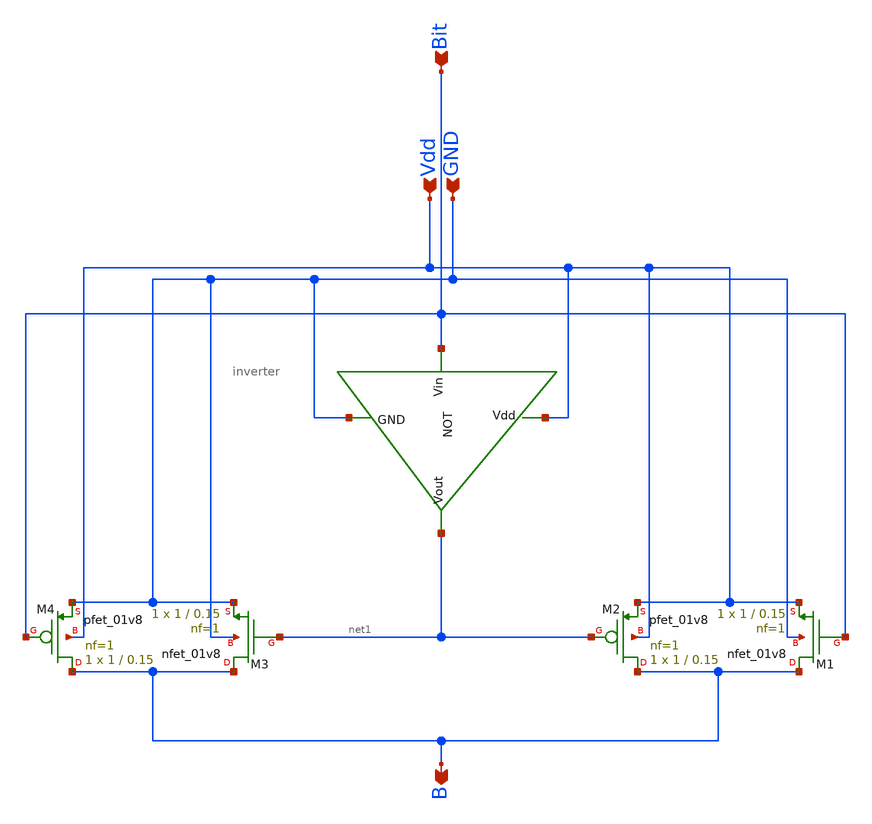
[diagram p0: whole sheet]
** sch_path: MUX_2to1.sch
**.subckt MUX_2to1 Bit Vdd GND B
*.ipin Bit
*.ipin Vdd
*.ipin GND
*.opin B
XM1 B Bit Vdd GND sky130_fd_pr__nfet_01v8 L=0.15 W=1 nf=1 ad='int((1 + 1)/2) * 1 / 1 * 0.29' as='int((1 + 2)/2) * 1 / 1 * 0.29'
+ pd='2*int((1 + 1)/2) * (1 / 1 + 0.29)' ps='2*int((1 + 2)/2) * (1 / 1 + 0.29)' nrd='0.29 / 1 ' nrs='0.29 / 1 '
+ sa=0 sb=0 sd=0 mult=1 m=1
XM2 B net1 Vdd Vdd sky130_fd_pr__pfet_01v8 L=0.15 W=1 nf=1 ad='int((1 + 1)/2) * 1 / 1 * 0.29' as='int((1 + 2)/2) * 1 / 1 * 0.29'
+ pd='2*int((1 + 1)/2) * (1 / 1 + 0.29)' ps='2*int((1 + 2)/2) * (1 / 1 + 0.29)' nrd='0.29 / 1 ' nrs='0.29 / 1 '
+ sa=0 sb=0 sd=0 mult=1 m=1
x1 Vdd Bit net1 GND inverter
XM3 B net1 GND GND sky130_fd_pr__nfet_01v8 L=0.15 W=1 nf=1 ad='int((1 + 1)/2) * 1 / 1 * 0.29' as='int((1 + 2)/2) * 1 / 1 * 0.29'
+ pd='2*int((1 + 1)/2) * (1 / 1 + 0.29)' ps='2*int((1 + 2)/2) * (1 / 1 + 0.29)' nrd='0.29 / 1 ' nrs='0.29 / 1 '
+ sa=0 sb=0 sd=0 mult=1 m=1
XM4 B Bit GND Vdd sky130_fd_pr__pfet_01v8 L=0.15 W=1 nf=1 ad='int((1 + 1)/2) * 1 / 1 * 0.29' as='int((1 + 2)/2) * 1 / 1 * 0.29'
+ pd='2*int((1 + 1)/2) * (1 / 1 + 0.29)' ps='2*int((1 + 2)/2) * (1 / 1 + 0.29)' nrd='0.29 / 1 ' nrs='0.29 / 1 '
+ sa=0 sb=0 sd=0 mult=1 m=1
**.ends

* expanding   symbol:  /home/jetha/Projects/sky130/SAR_ADC/inverter/inverter.sym # of pins=4
** sym_path: inverter.sym
** sch_path: inverter.sch
.subckt inverter Vdd Vin Vout GND
*.ipin Vin
*.ipin Vdd
*.ipin GND
*.opin Vout
XM2 Vout Vin GND GND sky130_fd_pr__nfet_01v8 L=0.15 W=1 nf=1 ad='int((1 + 1)/2) * 1 / 1 * 0.29' as='int((1 + 2)/2) * 1 / 1 * 0.29'
+ pd='2*int((1 + 1)/2) * (1 / 1 + 0.29)' ps='2*int((1 + 2)/2) * (1 / 1 + 0.29)' nrd='0.29 / 1 ' nrs='0.29 / 1 '
+ sa=0 sb=0 sd=0 mult=1 m=1
XM1 Vout Vin Vdd Vdd sky130_fd_pr__pfet_01v8 L=0.15 W=2 nf=1 ad='int((1 + 1)/2) * 2 / 1 * 0.29' as='int((1 + 2)/2) * 2 / 1 * 0.29'
+ pd='2*int((1 + 1)/2) * (2 / 1 + 0.29)' ps='2*int((1 + 2)/2) * (2 / 1 + 0.29)' nrd='0.29 / 2 ' nrs='0.29 / 2 '
+ sa=0 sb=0 sd=0 mult=1 m=1
.ends

.end
